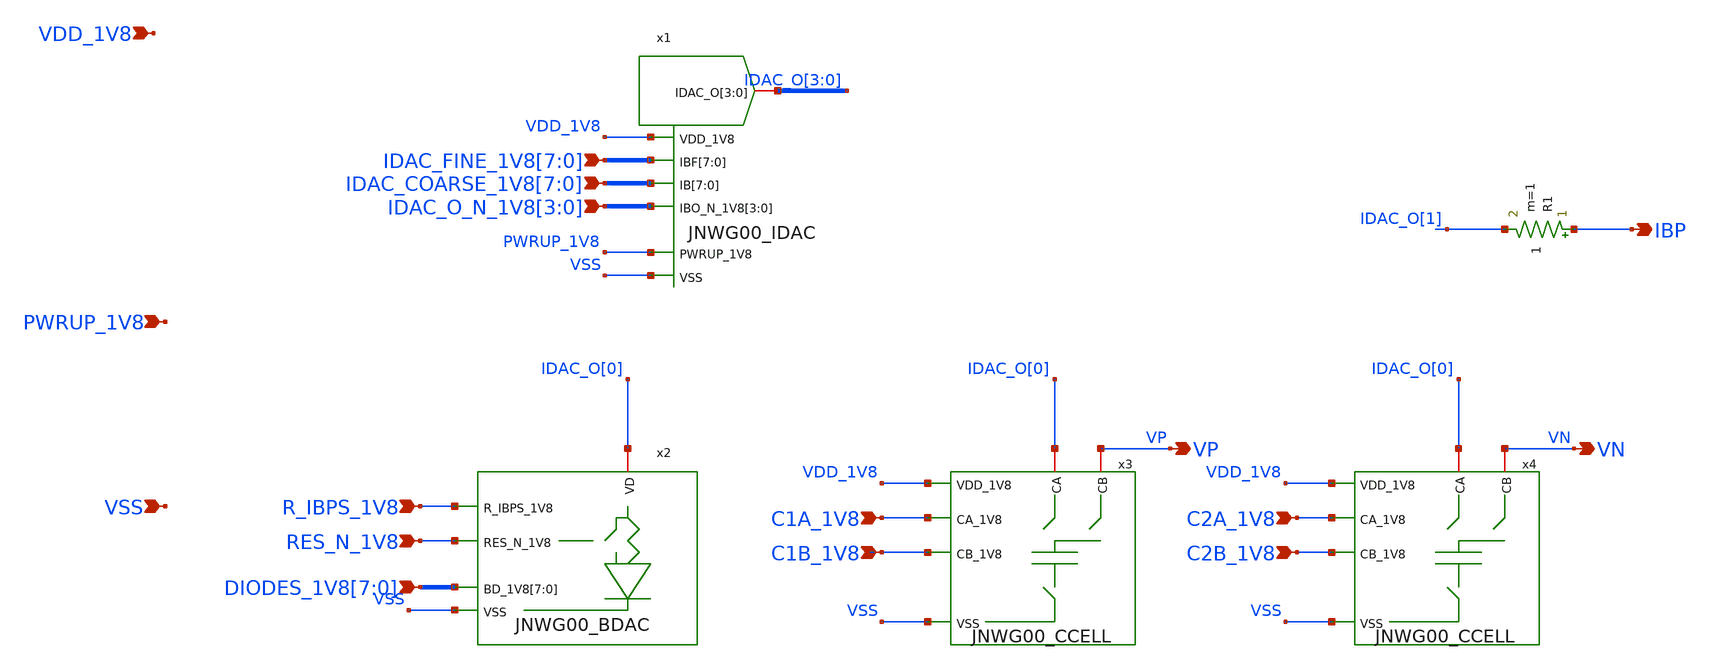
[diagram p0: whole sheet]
** sch_path: design/JNW_GR00_SKY130NM/JNWG00_CORE.sch
**.subckt JNWG00_CORE VDD_1V8 VSS
*+ IDAC_FINE_1V8[7],IDAC_FINE_1V8[6],IDAC_FINE_1V8[5],IDAC_FINE_1V8[4],IDAC_FINE_1V8[3],IDAC_FINE_1V8[2],IDAC_FINE_1V8[1],IDAC_FINE_1V8[0]
*+ IDAC_COARSE_1V8[7],IDAC_COARSE_1V8[6],IDAC_COARSE_1V8[5],IDAC_COARSE_1V8[4],IDAC_COARSE_1V8[3],IDAC_COARSE_1V8[2],IDAC_COARSE_1V8[1],IDAC_COARSE_1V8[0] IDAC_O_N_1V8[3],IDAC_O_N_1V8[2],IDAC_O_N_1V8[1],IDAC_O_N_1V8[0] RES_N_1V8
*+ DIODES_1V8[7],DIODES_1V8[6],DIODES_1V8[5],DIODES_1V8[4],DIODES_1V8[3],DIODES_1V8[2],DIODES_1V8[1],DIODES_1V8[0] C1A_1V8 C1B_1V8 C2A_1V8 C2B_1V8 VP VN PWRUP_1V8 IBP R_IBPS_1V8
*.ipin VDD_1V8
*.ipin VSS
*.ipin
*+ IDAC_FINE_1V8[7],IDAC_FINE_1V8[6],IDAC_FINE_1V8[5],IDAC_FINE_1V8[4],IDAC_FINE_1V8[3],IDAC_FINE_1V8[2],IDAC_FINE_1V8[1],IDAC_FINE_1V8[0]
*.ipin
*+ IDAC_COARSE_1V8[7],IDAC_COARSE_1V8[6],IDAC_COARSE_1V8[5],IDAC_COARSE_1V8[4],IDAC_COARSE_1V8[3],IDAC_COARSE_1V8[2],IDAC_COARSE_1V8[1],IDAC_COARSE_1V8[0]
*.ipin IDAC_O_N_1V8[3],IDAC_O_N_1V8[2],IDAC_O_N_1V8[1],IDAC_O_N_1V8[0]
*.ipin RES_N_1V8
*.ipin
*+ DIODES_1V8[7],DIODES_1V8[6],DIODES_1V8[5],DIODES_1V8[4],DIODES_1V8[3],DIODES_1V8[2],DIODES_1V8[1],DIODES_1V8[0]
*.ipin C1A_1V8
*.ipin C1B_1V8
*.ipin C2A_1V8
*.ipin C2B_1V8
*.opin VP
*.opin VN
*.ipin PWRUP_1V8
*.opin IBP
*.ipin R_IBPS_1V8
x2 DIODES_1V8[7] DIODES_1V8[6] DIODES_1V8[5] DIODES_1V8[4] DIODES_1V8[3] DIODES_1V8[2] DIODES_1V8[1]
+ DIODES_1V8[0] IDAC_O[0] VSS RES_N_1V8 R_IBPS_1V8 JNWG00_BDAC
x1 IDAC_FINE_1V8[7] IDAC_FINE_1V8[6] IDAC_FINE_1V8[5] IDAC_FINE_1V8[4] IDAC_FINE_1V8[3]
+ IDAC_FINE_1V8[2] IDAC_FINE_1V8[1] IDAC_FINE_1V8[0] IDAC_COARSE_1V8[7] IDAC_COARSE_1V8[6] IDAC_COARSE_1V8[5]
+ IDAC_COARSE_1V8[4] IDAC_COARSE_1V8[3] IDAC_COARSE_1V8[2] IDAC_COARSE_1V8[1] IDAC_COARSE_1V8[0] VDD_1V8 IDAC_O[3]
+ IDAC_O[2] IDAC_O[1] IDAC_O[0] IDAC_O_N_1V8[3] IDAC_O_N_1V8[2] IDAC_O_N_1V8[1] IDAC_O_N_1V8[0] PWRUP_1V8 VSS
+ JNWG00_IDAC
x3 VDD_1V8 IDAC_O[0] C1A_1V8 VSS VP C1B_1V8 JNWG00_CCELL
x4 VDD_1V8 IDAC_O[0] C2A_1V8 VSS VN C2B_1V8 JNWG00_CCELL
R1 IBP IDAC_O[1] 1 m=1
**.ends
.end
